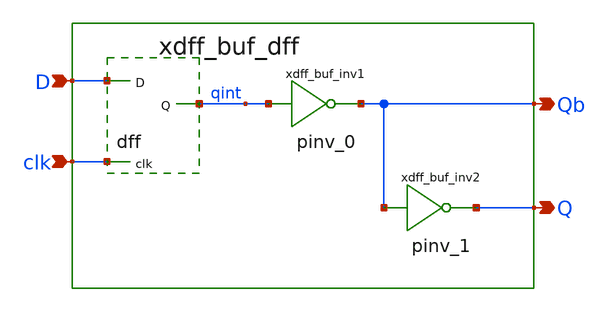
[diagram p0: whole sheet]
** sch_path: sram_2_16_scn4m/dff_buf_0.sch
**.subckt dff_buf_0 D Q Qb clk
*.ipin D
*.opin Q
*.opin Qb
*.ipin clk
xdff_buf_dff D qint clk vdd gnd dff
xdff_buf_inv1 qint Qb vdd gnd pinv_0
xdff_buf_inv2 Qb Q vdd gnd pinv_1
**.ends

* expanding   symbol:  dff.sym # of pins=3
** sym_path: sram_2_64_scn4m_lcc/dff.sym
** sch_path: sram_2_64_scn4m_lcc/dff.sch
.subckt dff D Q clk vdd gnd
*.ipin D
*.ipin clk
*.opin Q
M1013 net1 a_24_24# net2 gnd n w=5u l=0.18u m=1
M1012 net2 D gnd gnd n w=2u l=0.4u m=1
M1001 net3 D vdd vdd p w=4u l=0.4u m=1
M1002 net1 clk net3 vdd p w=4u l=0.4u m=1
M1000 a_24_24# clk vdd vdd p w=8u l=0.4u m=1
M1010 a_24_24# clk gnd gnd n w=4u l=0.4u m=1
M1005 a_152_16# net1 vdd vdd p w=4u l=0.4u m=1
M1016 a_152_16# net1 gnd gnd n w=5u l=0.4u m=1
M1004 net5 a_152_16# vdd vdd p w=4u l=0.4u m=1
M1003 net1 a_24_24# net5 vdd p w=4u l=0.4u m=1
M1014 net1 clk net4 gnd n w=2u l=0.4u m=1
M1015 net4 a_152_16# gnd gnd n w=2u l=0.4u m=1
M1006 net8 a_152_16# vdd vdd p w=4u l=0.4u m=1
M1007 net6 a_24_24# net8 vdd p w=4u l=0.4u m=1
M1018 net6 clk net7 gnd n w=2u l=0.4u m=1
M1017 net7 a_152_16# gnd gnd n w=2u l=0.4u m=1
M1021 Q net6 gnd gnd n w=4u l=0.4u m=1
M1011 Q net6 vdd vdd p w=8u l=0.4u m=1
M1020 net9 Q gnd gnd n w=2u l=0.4u m=1
M1019 net6 a_24_24# net9 gnd n w=2u l=0.4u m=1
M1009 net10 Q vdd vdd p w=2u l=0.4u m=1
M1008 net6 clk net10 vdd p w=2u l=0.4u m=1
.ends


* expanding   symbol:  pinv_0.sym # of pins=2
** sym_path: sram_2_16_scn4m/pinv_0.sym
** sch_path: sram_2_16_scn4m/pinv_0.sch
.subckt pinv_0 A Z vdd gnd
*.ipin A
*.opin Z
Mpinv_nmos Z A gnd gnd n w=1.6u l=0.4u m=1
Mp_inv_pmos Z A vdd vdd p w=3.2u l=0.4u m=1
.ends


* expanding   symbol:  pinv_1.sym # of pins=2
** sym_path: sram_2_64_scn4m_lcc/pinv_1.sym
** sch_path: sram_2_64_scn4m_lcc/pinv_1.sch
.subckt pinv_1 A Z vdd gnd
*.ipin A
*.opin Z
Mpinv_nmos Z A gnd gnd n w=0.8u l=0.4u m=1
Mp_inv_pmos Z A vdd vdd p w=6.4u l=0.4u m=1
.ends

.end
